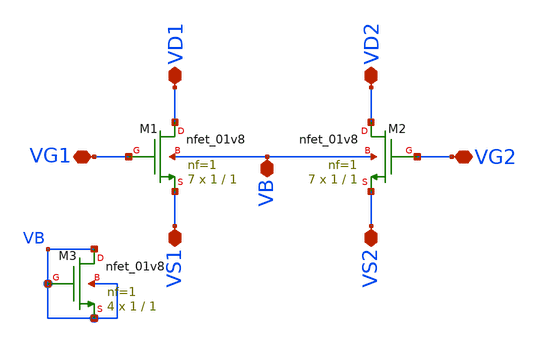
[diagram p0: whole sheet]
** sch_path: xschem/INA_layout_v2/nfets.sch
**.subckt nfets VS1 VS2 VB VG1 VG2 VD1 VD2
*.iopin VS1
*.iopin VS2
*.iopin VB
*.iopin VG1
*.iopin VG2
*.iopin VD1
*.iopin VD2
XM1 VD1 VG1 VS1 VB sky130_fd_pr__nfet_01v8 L=1 W=1 nf=1 ad='int((nf+1)/2) * W/nf * 0.29' as='int((nf+2)/2) * W/nf * 0.29'
+ pd='2*int((nf+1)/2) * (W/nf + 0.29)' ps='2*int((nf+2)/2) * (W/nf + 0.29)' nrd='0.29 / W' nrs='0.29 / W'
+ sa=0 sb=0 sd=0 mult=7 m=7
XM2 VD2 VG2 VS2 VB sky130_fd_pr__nfet_01v8 L=1 W=1 nf=1 ad='int((nf+1)/2) * W/nf * 0.29' as='int((nf+2)/2) * W/nf * 0.29'
+ pd='2*int((nf+1)/2) * (W/nf + 0.29)' ps='2*int((nf+2)/2) * (W/nf + 0.29)' nrd='0.29 / W' nrs='0.29 / W'
+ sa=0 sb=0 sd=0 mult=7 m=7
XM3 VB VB VB VB sky130_fd_pr__nfet_01v8 L=1 W=1 nf=1 ad='int((nf+1)/2) * W/nf * 0.29' as='int((nf+2)/2) * W/nf * 0.29'
+ pd='2*int((nf+1)/2) * (W/nf + 0.29)' ps='2*int((nf+2)/2) * (W/nf + 0.29)' nrd='0.29 / W' nrs='0.29 / W'
+ sa=0 sb=0 sd=0 mult=4 m=4
**.ends
.end
